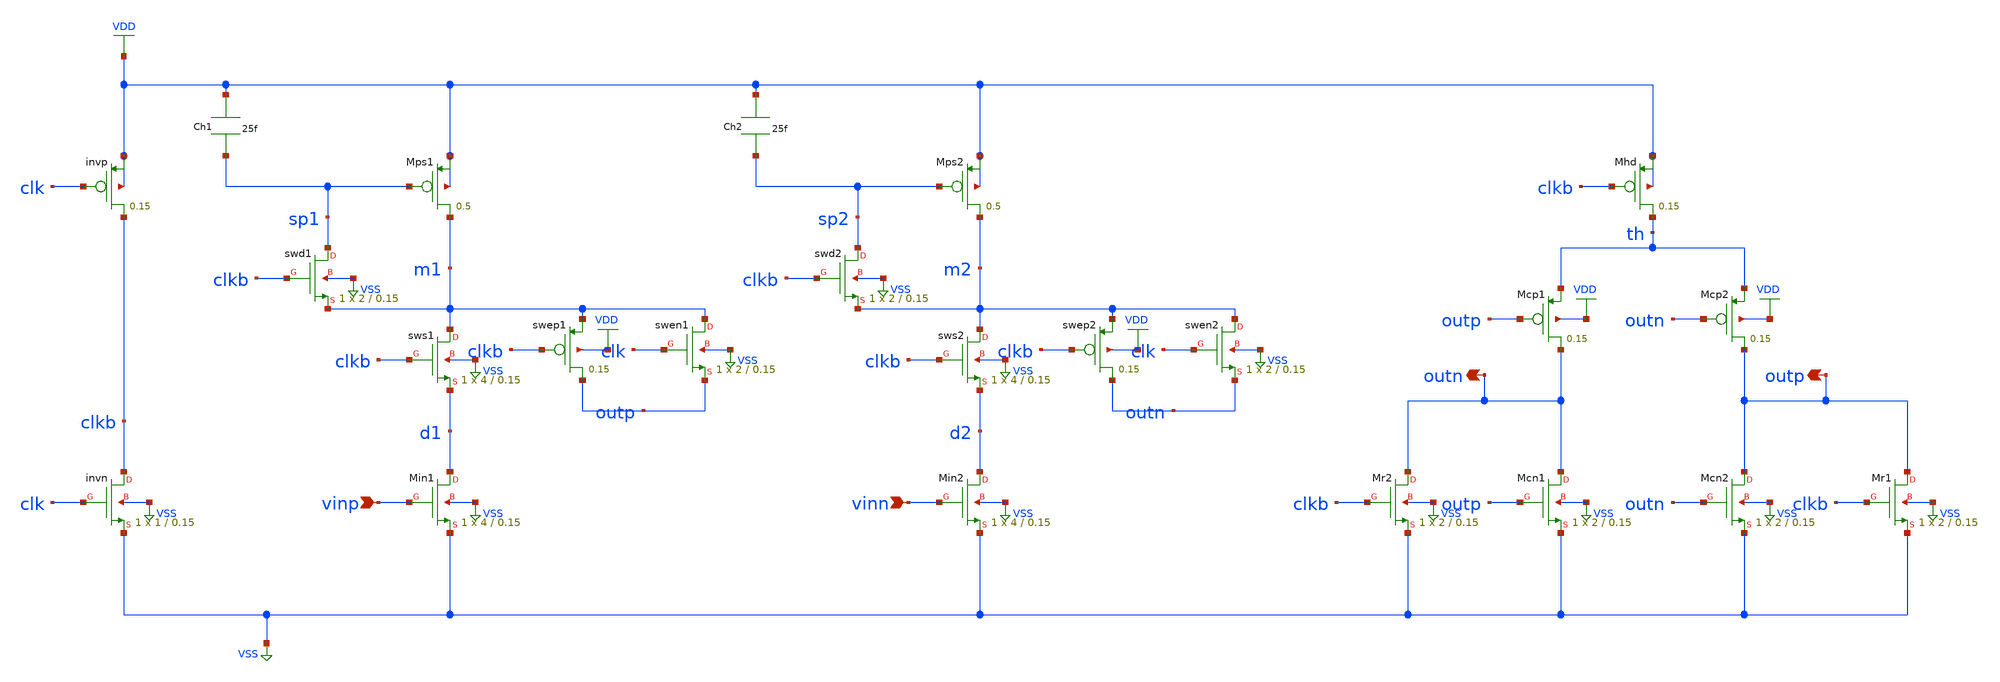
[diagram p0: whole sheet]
** sch_path: eda/hero/schematics/current_sampling.sch
**.subckt current_sampling vinp vinn outn outp
*.ipin vinp
*.ipin vinn
*.opin outn
*.opin outp
Xinvp clkb clk VDD VDD sky130_fd_pr__sky130_fd_pr__pfet_01v8 L=0.15 W=2 nrd='0.29 / W' nrs='0.29 / W'
+ sa=0 sb=0 sd=0 mult=1 m=1
Xinvn clkb clk VSS VSS sky130_fd_pr__sky130_fd_pr__nfet_01v8 L=0.15 W=1 nrd='0.29 / W' nrs='0.29 / W'
+ sa=0 sb=0 sd=0 mult=1 m=1
XMps1 m1 sp1 VDD VDD sky130_fd_pr__sky130_fd_pr__pfet_01v8 L=0.5 W=16 nrd='0.29 / W' nrs='0.29 / W' sa=0
+ sb=0 sd=0 mult=1 m=1
Xswd1 sp1 clkb m1 VSS sky130_fd_pr__sky130_fd_pr__nfet_01v8 L=0.15 W=2 nrd='0.29 / W' nrs='0.29 / W'
+ sa=0 sb=0 sd=0 mult=1 m=1
Xsws1 m1 clkb d1 VSS sky130_fd_pr__sky130_fd_pr__nfet_01v8 L=0.15 W=4 nrd='0.29 / W' nrs='0.29 / W' sa=0
+ sb=0 sd=0 mult=1 m=1
XMin1 d1 vinp VSS VSS sky130_fd_pr__sky130_fd_pr__nfet_01v8 L=0.15 W=4 nrd='0.29 / W' nrs='0.29 / W'
+ sa=0 sb=0 sd=0 mult=1 m=1
Xswep1 outp clkb m1 VDD sky130_fd_pr__sky130_fd_pr__pfet_01v8 L=0.15 W=4 nrd='0.29 / W' nrs='0.29 / W'
+ sa=0 sb=0 sd=0 mult=1 m=1
Xswen1 m1 clk outp VSS sky130_fd_pr__sky130_fd_pr__nfet_01v8 L=0.15 W=2 nrd='0.29 / W' nrs='0.29 / W'
+ sa=0 sb=0 sd=0 mult=1 m=1
XMps2 m2 sp2 VDD VDD sky130_fd_pr__sky130_fd_pr__pfet_01v8 L=0.5 W=16 nrd='0.29 / W' nrs='0.29 / W' sa=0
+ sb=0 sd=0 mult=1 m=1
Xswd2 sp2 clkb m2 VSS sky130_fd_pr__sky130_fd_pr__nfet_01v8 L=0.15 W=2 nrd='0.29 / W' nrs='0.29 / W'
+ sa=0 sb=0 sd=0 mult=1 m=1
Xsws2 m2 clkb d2 VSS sky130_fd_pr__sky130_fd_pr__nfet_01v8 L=0.15 W=4 nrd='0.29 / W' nrs='0.29 / W' sa=0
+ sb=0 sd=0 mult=1 m=1
XMin2 d2 vinn VSS VSS sky130_fd_pr__sky130_fd_pr__nfet_01v8 L=0.15 W=4 nrd='0.29 / W' nrs='0.29 / W'
+ sa=0 sb=0 sd=0 mult=1 m=1
Xswep2 outn clkb m2 VDD sky130_fd_pr__sky130_fd_pr__pfet_01v8 L=0.15 W=4 nrd='0.29 / W' nrs='0.29 / W'
+ sa=0 sb=0 sd=0 mult=1 m=1
Xswen2 m2 clk outn VSS sky130_fd_pr__sky130_fd_pr__nfet_01v8 L=0.15 W=2 nrd='0.29 / W' nrs='0.29 / W'
+ sa=0 sb=0 sd=0 mult=1 m=1
XMhd th clkb VDD VDD sky130_fd_pr__sky130_fd_pr__pfet_01v8 L=0.15 W=4 nrd='0.29 / W' nrs='0.29 / W' sa=0
+ sb=0 sd=0 mult=1 m=1
XMcp1 outn outp th VDD sky130_fd_pr__sky130_fd_pr__pfet_01v8 L=0.15 W=2 nrd='0.29 / W' nrs='0.29 / W'
+ sa=0 sb=0 sd=0 mult=1 m=1
XMcp2 outp outn th VDD sky130_fd_pr__sky130_fd_pr__pfet_01v8 L=0.15 W=2 nrd='0.29 / W' nrs='0.29 / W'
+ sa=0 sb=0 sd=0 mult=1 m=1
XMr2 outn clkb VSS VSS sky130_fd_pr__sky130_fd_pr__nfet_01v8 L=0.15 W=2 nrd='0.29 / W' nrs='0.29 / W'
+ sa=0 sb=0 sd=0 mult=1 m=1
XMcn1 outn outp VSS VSS sky130_fd_pr__sky130_fd_pr__nfet_01v8 L=0.15 W=2 nrd='0.29 / W' nrs='0.29 / W'
+ sa=0 sb=0 sd=0 mult=1 m=1
XMcn2 outp outn VSS VSS sky130_fd_pr__sky130_fd_pr__nfet_01v8 L=0.15 W=2 nrd='0.29 / W' nrs='0.29 / W'
+ sa=0 sb=0 sd=0 mult=1 m=1
XMr1 outp clkb VSS VSS sky130_fd_pr__sky130_fd_pr__nfet_01v8 L=0.15 W=2 nrd='0.29 / W' nrs='0.29 / W'
+ sa=0 sb=0 sd=0 mult=1 m=1
Ch1 VDD sp1 25f m=1
Ch2 VDD sp2 25f m=1
**.ends
.GLOBAL VSS
.GLOBAL VDD
.end
